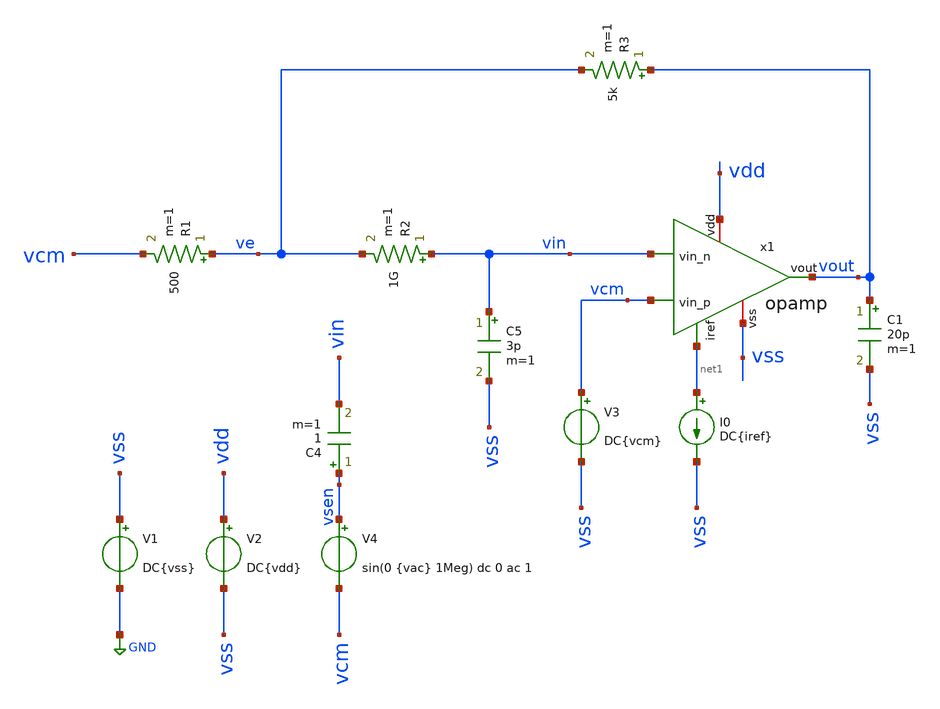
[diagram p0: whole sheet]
** sch_path: tb_opamp_openloop.sch
**.subckt tb_opamp_openloop
V1 vss GND DC{vss}
V2 vdd vss DC{vdd}
V3 vcm vss DC{vcm}
V4 vsen vcm sin(0 {vac} 1Meg) dc 0 ac 1
C4 vsen vin 1 m=1
I0 net1 vss DC{iref}
R1 ve vcm 500 m=1
R2 vin ve 1G m=1
R3 vout ve 5k m=1
C5 vin vss 3p m=1
C1 vout vss 20p m=1
x1 vdd net1 vin vcm vout vss opamp
**** begin user architecture code




* Circuit Parameters
.param vss  = 0.0
.param vac  = 60m
.param w857 = 15
.param l857 = 0.9
.param m857 = 1.2
.param wpar = 30
.param lpar = 0.45
.param mpar = 15
.param w34  = 6
.param l34  = 2
.param m34  = 6
.param w6   = 20
.param l6   = 1.5
.param m6   = 15

* Corner Dependant Parameters
.param vdd  = 1.8
.param vcm  = 0.8
.param iref = 100u
.options TEMP = 65.0

* Include Models
.lib ~/skywater/skywater-pdk/libraries/sky130_fd_pr_ngspice/latest/models/corners/sky130.lib TT

* OP Parameters & Singals to save
.save all  @M.X1.XM1.msky130_fd_pr__pfet_01v8_lvt[id] @M.X1.XM1.msky130_fd_pr__pfet_01v8_lvt[vth] @M.X1.XM1.msky130_fd_pr__pfet_01v8_lvt[vgs] @M.X1.XM1.msky130_fd_pr__pfet_01v8_lvt[vds] @M.X1.XM1.msky130_fd_pr__pfet_01v8_lvt[vdsat] @M.X1.XM1.msky130_fd_pr__pfet_01v8_lvt[gm] @M.X1.XM1.msky130_fd_pr__pfet_01v8_lvt[gds] @M.X1.XM1.msky130_fd_pr__pfet_01v8_lvt[cgg]  @M.X1.XM2.msky130_fd_pr__pfet_01v8_lvt[id] @M.X1.XM2.msky130_fd_pr__pfet_01v8_lvt[vth] @M.X1.XM2.msky130_fd_pr__pfet_01v8_lvt[vgs] @M.X1.XM2.msky130_fd_pr__pfet_01v8_lvt[vds] @M.X1.XM2.msky130_fd_pr__pfet_01v8_lvt[vdsat] @M.X1.XM2.msky130_fd_pr__pfet_01v8_lvt[gm] @M.X1.XM2.msky130_fd_pr__pfet_01v8_lvt[gds] @M.X1.XM2.msky130_fd_pr__pfet_01v8_lvt[cgg]  @M.X1.XM3.msky130_fd_pr__nfet_01v8[id] @M.X1.XM3.msky130_fd_pr__nfet_01v8[vth] @M.X1.XM3.msky130_fd_pr__nfet_01v8[vgs] @M.X1.XM3.msky130_fd_pr__nfet_01v8[vds] @M.X1.XM3.msky130_fd_pr__nfet_01v8[vdsat] @M.X1.XM3.msky130_fd_pr__nfet_01v8[gm] @M.X1.XM3.msky130_fd_pr__nfet_01v8[gds] @M.X1.XM3.msky130_fd_pr__nfet_01v8[cgg]  @M.X1.XM4.msky130_fd_pr__nfet_01v8[id] @M.X1.XM4.msky130_fd_pr__nfet_01v8[vth] @M.X1.XM4.msky130_fd_pr__nfet_01v8[vgs] @M.X1.XM4.msky130_fd_pr__nfet_01v8[vds] @M.X1.XM4.msky130_fd_pr__nfet_01v8[vdsat] @M.X1.XM4.msky130_fd_pr__nfet_01v8[gm] @M.X1.XM4.msky130_fd_pr__nfet_01v8[gds] @M.X1.XM4.msky130_fd_pr__nfet_01v8[cgg]  @M.X1.XM5.msky130_fd_pr__pfet_01v8[id] @M.X1.XM5.msky130_fd_pr__pfet_01v8[vth] @M.X1.XM5.msky130_fd_pr__pfet_01v8[vgs] @M.X1.XM5.msky130_fd_pr__pfet_01v8[vds] @M.X1.XM5.msky130_fd_pr__pfet_01v8[vdsat] @M.X1.XM5.msky130_fd_pr__pfet_01v8[gm] @M.X1.XM5.msky130_fd_pr__pfet_01v8[gds] @M.X1.XM5.msky130_fd_pr__pfet_01v8[cgg]  @M.X1.XM6.msky130_fd_pr__nfet_01v8[id] @M.X1.XM6.msky130_fd_pr__nfet_01v8[vth] @M.X1.XM6.msky130_fd_pr__nfet_01v8[vgs] @M.X1.XM6.msky130_fd_pr__nfet_01v8[vds] @M.X1.XM6.msky130_fd_pr__nfet_01v8[vdsat] @M.X1.XM6.msky130_fd_pr__nfet_01v8[gm] @M.X1.XM6.msky130_fd_pr__nfet_01v8[gds] @M.X1.XM6.msky130_fd_pr__nfet_01v8[cgg]  @M.X1.XM7.msky130_fd_pr__pfet_01v8[id] @M.X1.XM7.msky130_fd_pr__pfet_01v8[vth] @M.X1.XM7.msky130_fd_pr__pfet_01v8[vgs] @M.X1.XM7.msky130_fd_pr__pfet_01v8[vds] @M.X1.XM7.msky130_fd_pr__pfet_01v8[vdsat] @M.X1.XM7.msky130_fd_pr__pfet_01v8[gm] @M.X1.XM7.msky130_fd_pr__pfet_01v8[gds] @M.X1.XM7.msky130_fd_pr__pfet_01v8[cgg]  @M.X1.XM8.msky130_fd_pr__pfet_01v8[id] @M.X1.XM8.msky130_fd_pr__pfet_01v8[vth] @M.X1.XM8.msky130_fd_pr__pfet_01v8[vgs] @M.X1.XM8.msky130_fd_pr__pfet_01v8[vds] @M.X1.XM8.msky130_fd_pr__pfet_01v8[vdsat] @M.X1.XM8.msky130_fd_pr__pfet_01v8[gm] @M.X1.XM8.msky130_fd_pr__pfet_01v8[gds] @M.X1.XM8.msky130_fd_pr__pfet_01v8[cgg]  @M.X1.XM9.msky130_fd_pr__nfet_01v8[id] @M.X1.XM9.msky130_fd_pr__nfet_01v8[vth] @M.X1.XM9.msky130_fd_pr__nfet_01v8[vgs] @M.X1.XM9.msky130_fd_pr__nfet_01v8[vds] @M.X1.XM9.msky130_fd_pr__nfet_01v8[vdsat] @M.X1.XM9.msky130_fd_pr__nfet_01v8[gm] @M.X1.XM9.msky130_fd_pr__nfet_01v8[gds] @M.X1.XM9.msky130_fd_pr__nfet_01v8[cgg]

*Simulation
.control
  set color0 = white

  ac dec 100 1 10G
  setplot ac1
  meas ac GBW when vdb(vout)=0
  meas ac DCG find vdb(vout) at=1]]
  meas ac PM find vp(vout) when vdb(vout)=0
  print PM*180/PI
  meas ac GM find vdb(vout) when vp(vout)=0
  plot vdb(vout) {vp(vout)*180/PI}
  write tb_opamp_openloop_ac1.raw

  reset
  op
  setplot op1
  unset filetype
  write tb_opamp_openloop.raw

.endc

.end


**** end user architecture code
**.ends

* expanding   symbol:  opamp.sym # of pins=6
** sym_path: opamp.sym
** sch_path: opamp.sch
.subckt opamp vdd iref vin_n vin_p vout vss
*.iopin vdd
*.iopin vss
*.ipin vin_n
*.ipin vin_p
*.ipin iref
*.opin vout
XM3 vbn vbn vss vss sky130_fd_pr__nfet_01v8 L={l34} W={w34} nf=1 ad='W * 0.29' as='W * 0.29' pd='2 * (W + 0.29)'
+ ps='2 * (W + 0.29)' nrd='0.29 / W' nrs='0.29 / W' sa=0 sb=0 sd=0 mult={m34} m={m34}
XM4 voe1 vbn vss vss sky130_fd_pr__nfet_01v8 L={l34} W={w34} nf=1 ad='W * 0.29' as='W * 0.29' pd='2 * (W + 0.29)'
+ ps='2 * (W + 0.29)' nrd='0.29 / W' nrs='0.29 / W' sa=0 sb=0 sd=0 mult={m34} m={m34}
XM5 vp iref vdd vdd sky130_fd_pr__pfet_01v8 L={l857} W={w857} nf=1 ad='W * 0.29' as='W * 0.29' pd='2 * (W + 0.29)'
+ ps='2 * (W + 0.29)' nrd='0.29 / W' nrs='0.29 / W' sa=0 sb=0 sd=0 mult=20 m=20
XM7 vout iref vdd vdd sky130_fd_pr__pfet_01v8 L={l857} W={w857} nf=1 ad='W * 0.29' as='W * 0.29' pd='2 * (W + 0.29)'
+ ps='2 * (W + 0.29)' nrd='0.29 / W' nrs='0.29 / W' sa=0 sb=0 sd=0 mult=200 m=200
XM8 iref iref vdd vdd sky130_fd_pr__pfet_01v8 L={l857} W={w857} nf=1 ad='W * 0.29' as='W * 0.29' pd='2 * (W + 0.29)'
+ ps='2 * (W + 0.29)' nrd='0.29 / W' nrs='0.29 / W' sa=0 sb=0 sd=0 mult=10 m=10
XM9 net1 vdd voe1 vss sky130_fd_pr__nfet_01v8 L=0.4 W=3 nf=1 ad='W * 0.29' as='W * 0.29' pd='2 * (W + 0.29)'
+ ps='2 * (W + 0.29)' nrd='0.29 / W' nrs='0.29 / W' sa=0 sb=0 sd=0 mult=3 m=3
XM6 vout voe1 vss vss sky130_fd_pr__nfet_01v8 L={l6} W={w6} nf=1 ad='W * 0.29' as='W * 0.29' pd='2 * (W + 0.29)'
+ ps='2 * (W + 0.29)' nrd='0.29 / W' nrs='0.29 / W' sa=0 sb=0 sd=0 mult={m6} m={m6}
XM1 vbn vin_n vp vp sky130_fd_pr__pfet_01v8_lvt L={lpar} W={wpar} nf=1 ad='int((nf+1)/2) * W/nf * 0.29'
+ as='int((nf+2)/2) * W/nf * 0.29' pd='2*int((nf+1)/2) * (W/nf + 0.29)' ps='2*int((nf+2)/2) * (W/nf + 0.29)'
+ nrd='0.29 / W' nrs='0.29 / W' sa=0 sb=0 sd=0 mult={mpar} m={mpar}
XM2 voe1 vin_p vp vp sky130_fd_pr__pfet_01v8_lvt L={lpar} W={wpar} nf=1 ad='int((nf+1)/2) * W/nf * 0.29'
+ as='int((nf+2)/2) * W/nf * 0.29' pd='2*int((nf+1)/2) * (W/nf + 0.29)' ps='2*int((nf+2)/2) * (W/nf + 0.29)'
+ nrd='0.29 / W' nrs='0.29 / W' sa=0 sb=0 sd=0 mult={mpar} m={mpar}
C1 net1 vout 3.8p m=1
.ends

.GLOBAL GND
.end
